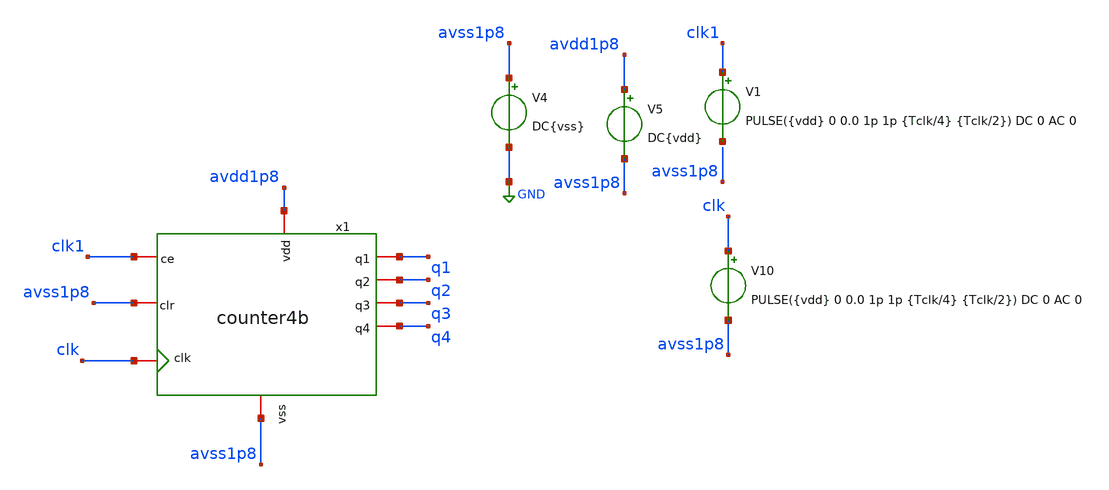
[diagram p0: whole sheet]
** sch_path: verification/testbenches/count4bits/tb_count4bits.sch
**.subckt tb_count4bits
x1 avdd1p8 avss1p8 q1 clk1 avss1p8 clk q2 q3 q4 counter4b
V4 avss1p8 GND DC{vss}
V10 clk avss1p8 PULSE({vdd} 0 0.0 1p 1p {Tclk/4} {Tclk/2}) DC 0 AC 0
V5 avdd1p8 avss1p8 DC{vdd}
V1 clk1 net1 PULSE({vdd} 0 0.0 1p 1p {Tclk/4} {Tclk/2}) DC 0 AC 0
**** begin user architecture code


* Circuit Parameters
.param vdd = 1.2
.param vss = 0.0
.param Tclk = 1000n
.param Tffd = 85n
.param Tclear = 165n
.options TEMP = 27.0
* Include Models - IHP SG13G2
.lib cornerMOSlv.lib mos_tt
* OP Parameters & Singals to save
.save all
*Simulations
.control
tran 0.01u 20000n
setplot tran1
plot v(clk) v(q1)+2.4 v(q2)+3.6 v(q3)+4.8 v(q4)+6.0
reset
dc V6 0 1.2 0.01
setplot dc
plot vin vout ylabel vout xlabel vin
set filetype = ascii
write dcsweep.raw
.endc
.end


**** end user architecture code
**.ends
.GLOBAL GND
.end
